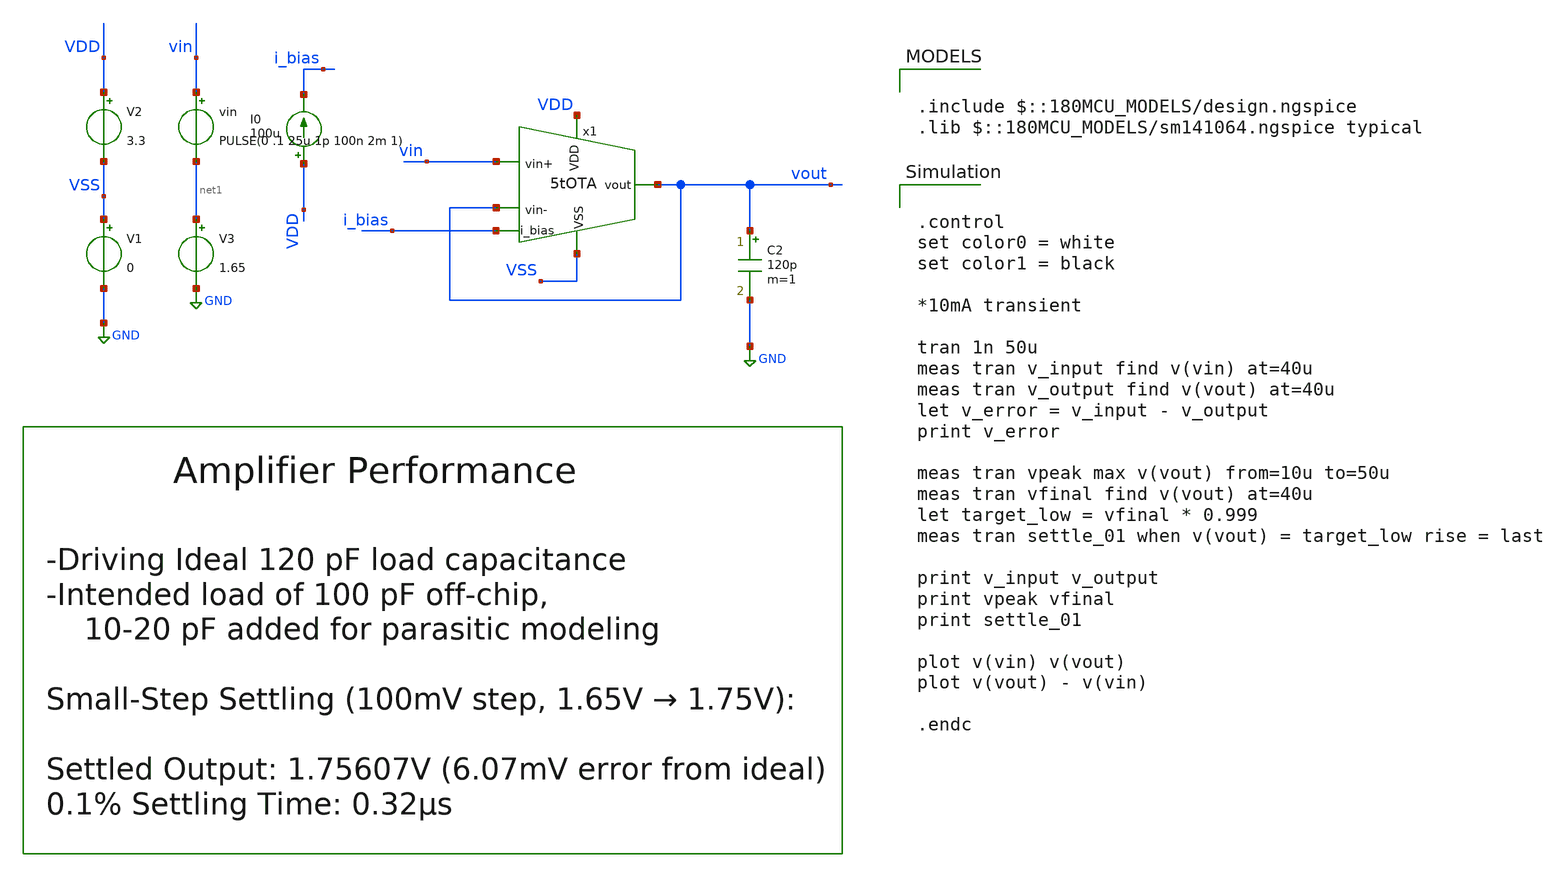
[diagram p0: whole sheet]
** sch_path: designs/libs/core_amps/ota_5t/tb/5tOTA_tb_tran_settle.sch
**.subckt 5tOTA_tb_tran_settle
V1 VSS GND 0
V2 VDD VSS 3.3
I0 VDD i_bias 100u
vin vin net1 PULSE(0 .1 25u 1p 100n 2m 1)
C2 vout GND 120p m=1
V3 net1 GND 1.65
x1 VDD vout vin vout i_bias VSS 5tOTA
**** begin user architecture code

.include $::180MCU_MODELS/design.ngspice
.lib $::180MCU_MODELS/sm141064.ngspice typical



.control
set color0 = white
set color1 = black

*10mA transient

tran 1n 50u
meas tran v_input find v(vin) at=40u
meas tran v_output find v(vout) at=40u
let v_error = v_input - v_output
print v_error

meas tran vpeak max v(vout) from=10u to=50u
meas tran vfinal find v(vout) at=40u
let target_low = vfinal * 0.999
meas tran settle_01 when v(vout) = target_low rise = last

print v_input v_output
print vpeak vfinal
print settle_01

plot v(vin) v(vout)
plot v(vout) - v(vin)

.endc


**** end user architecture code
**.ends

* expanding   symbol:  libs/core_amps/ota_5t/schem/5tOTA.sym # of pins=6
** sym_path: designs/5tOTA.sym
** sch_path: designs/5tOTA.sch
.subckt 5tOTA VDD vout vin+ vin- i_bias VSS
*.ipin VDD
*.opin vout
*.ipin i_bias
*.ipin vin+
*.ipin vin-
*.ipin VSS
XM1 net1 vin+ net2 VSS nfet_03v3 L=0.5u W=11.43u nf=1 ad='int((nf+1)/2) * W/nf * 0.18u' as='int((nf+2)/2) * W/nf * 0.18u'
+ pd='2*int((nf+1)/2) * (W/nf + 0.18u)' ps='2*int((nf+2)/2) * (W/nf + 0.18u)' nrd='0.18u / W' nrs='0.18u / W'
+ sa=0 sb=0 sd=0 m=1
XM2 vout vin- net2 VSS nfet_03v3 L=0.5u W=11.43u nf=1 ad='int((nf+1)/2) * W/nf * 0.18u' as='int((nf+2)/2) * W/nf * 0.18u'
+ pd='2*int((nf+1)/2) * (W/nf + 0.18u)' ps='2*int((nf+2)/2) * (W/nf + 0.18u)' nrd='0.18u / W' nrs='0.18u / W'
+ sa=0 sb=0 sd=0 m=1
XM3 net1 net1 VDD VDD pfet_03v3 L=0.5u W=22.86u nf=1 ad='int((nf+1)/2) * W/nf * 0.18u' as='int((nf+2)/2) * W/nf * 0.18u'
+ pd='2*int((nf+1)/2) * (W/nf + 0.18u)' ps='2*int((nf+2)/2) * (W/nf + 0.18u)' nrd='0.18u / W' nrs='0.18u / W'
+ sa=0 sb=0 sd=0 m=1
XM4 vout net1 VDD VDD pfet_03v3 L=0.5u W=22.86u nf=1 ad='int((nf+1)/2) * W/nf * 0.18u' as='int((nf+2)/2) * W/nf * 0.18u'
+ pd='2*int((nf+1)/2) * (W/nf + 0.18u)' ps='2*int((nf+2)/2) * (W/nf + 0.18u)' nrd='0.18u / W' nrs='0.18u / W'
+ sa=0 sb=0 sd=0 m=1
XM5 net2 i_bias VSS VSS nfet_03v3 L=0.5u W=22.86u nf=1 ad='int((nf+1)/2) * W/nf * 0.18u' as='int((nf+2)/2) * W/nf * 0.18u'
+ pd='2*int((nf+1)/2) * (W/nf + 0.18u)' ps='2*int((nf+2)/2) * (W/nf + 0.18u)' nrd='0.18u / W' nrs='0.18u / W'
+ sa=0 sb=0 sd=0 m=1
XM6 i_bias i_bias VSS VSS nfet_03v3 L=0.5u W=22.86u nf=1 ad='int((nf+1)/2) * W/nf * 0.18u' as='int((nf+2)/2) * W/nf * 0.18u'
+ pd='2*int((nf+1)/2) * (W/nf + 0.18u)' ps='2*int((nf+2)/2) * (W/nf + 0.18u)' nrd='0.18u / W' nrs='0.18u / W'
+ sa=0 sb=0 sd=0 m=1
.ends

.GLOBAL GND
.end
